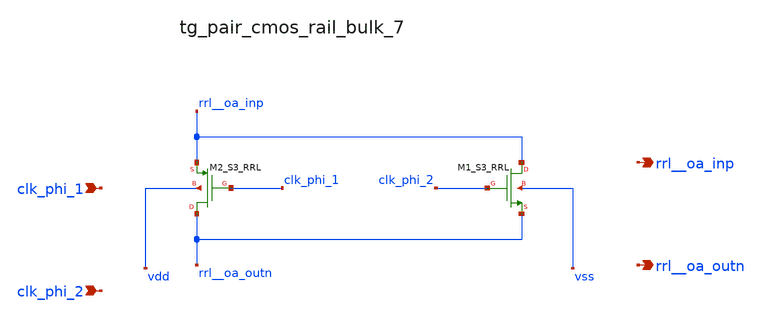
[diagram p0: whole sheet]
** sch_path: analog-db/raw/ia_004_fan_chopper_rrl/hier/blocks/tg_pair_cmos_rail_bulk_7.sch
**.subckt tg_pair_cmos_rail_bulk_7 clk_phi_1 clk_phi_2 rrl__oa_inp rrl__oa_outn
*.ipin clk_phi_1
*.ipin clk_phi_2
*.opin rrl__oa_inp
*.opin rrl__oa_outn
XM1_S3_RRL rrl__oa_inp clk_phi_2 rrl__oa_outn vss sg13_lv_nmos w=x_dut_xm1_s3_rrl_w
+ l=x_dut_xm1_s3_rrl_l ng=1 m=x_dut_xm1_s3_rrl_m
XM2_S3_RRL rrl__oa_outn clk_phi_1 rrl__oa_inp vdd sg13_lv_pmos w=x_dut_xm2_s3_rrl_w
+ l=x_dut_xm2_s3_rrl_l ng=1 m=x_dut_xm2_s3_rrl_m
**.ends
.end
